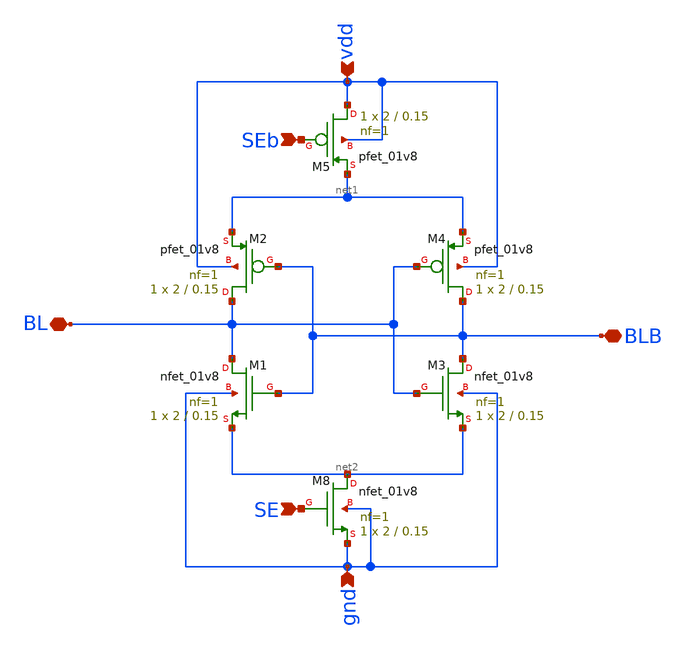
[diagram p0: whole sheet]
** sch_path: Projects/Schematic_Design_and_Analysis_of_an_8-Word_8-Bit_Static_RAM_with_6T_Storage_Cells_using_SKY130PDK/assets/schematic/sense_amp.sch
**.subckt sense_amp gnd vdd SE BLB BL SEb
*.ipin gnd
*.ipin vdd
*.ipin SE
*.iopin BLB
*.iopin BL
*.ipin SEb
XM1 BL BLB net2 gnd sky130_fd_pr__nfet_01v8 L=0.15 W=2 nf=1 ad='int((nf+1)/2) * W/nf * 0.29' as='int((nf+2)/2) * W/nf * 0.29'
+ pd='2*int((nf+1)/2) * (W/nf + 0.29)' ps='2*int((nf+2)/2) * (W/nf + 0.29)' nrd='0.29 / W' nrs='0.29 / W'
+ sa=0 sb=0 sd=0 mult=1 m=1
XM2 BL BLB net1 vdd sky130_fd_pr__pfet_01v8 L=0.15 W=2 nf=1 ad='int((nf+1)/2) * W/nf * 0.29' as='int((nf+2)/2) * W/nf * 0.29'
+ pd='2*int((nf+1)/2) * (W/nf + 0.29)' ps='2*int((nf+2)/2) * (W/nf + 0.29)' nrd='0.29 / W' nrs='0.29 / W'
+ sa=0 sb=0 sd=0 mult=1 m=1
XM3 BLB BL net2 gnd sky130_fd_pr__nfet_01v8 L=0.15 W=2 nf=1 ad='int((nf+1)/2) * W/nf * 0.29' as='int((nf+2)/2) * W/nf * 0.29'
+ pd='2*int((nf+1)/2) * (W/nf + 0.29)' ps='2*int((nf+2)/2) * (W/nf + 0.29)' nrd='0.29 / W' nrs='0.29 / W'
+ sa=0 sb=0 sd=0 mult=1 m=1
XM4 BLB BL net1 vdd sky130_fd_pr__pfet_01v8 L=0.15 W=2 nf=1 ad='int((nf+1)/2) * W/nf * 0.29' as='int((nf+2)/2) * W/nf * 0.29'
+ pd='2*int((nf+1)/2) * (W/nf + 0.29)' ps='2*int((nf+2)/2) * (W/nf + 0.29)' nrd='0.29 / W' nrs='0.29 / W'
+ sa=0 sb=0 sd=0 mult=1 m=1
XM8 net2 SE gnd gnd sky130_fd_pr__nfet_01v8 L=0.15 W=2 nf=1 ad='int((nf+1)/2) * W/nf * 0.29' as='int((nf+2)/2) * W/nf * 0.29'
+ pd='2*int((nf+1)/2) * (W/nf + 0.29)' ps='2*int((nf+2)/2) * (W/nf + 0.29)' nrd='0.29 / W' nrs='0.29 / W'
+ sa=0 sb=0 sd=0 mult=1 m=1
XM5 vdd SEb net1 vdd sky130_fd_pr__pfet_01v8 L=0.15 W=2 nf=1 ad='int((nf+1)/2) * W/nf * 0.29' as='int((nf+2)/2) * W/nf * 0.29'
+ pd='2*int((nf+1)/2) * (W/nf + 0.29)' ps='2*int((nf+2)/2) * (W/nf + 0.29)' nrd='0.29 / W' nrs='0.29 / W'
+ sa=0 sb=0 sd=0 mult=1 m=1
**.ends
.end
